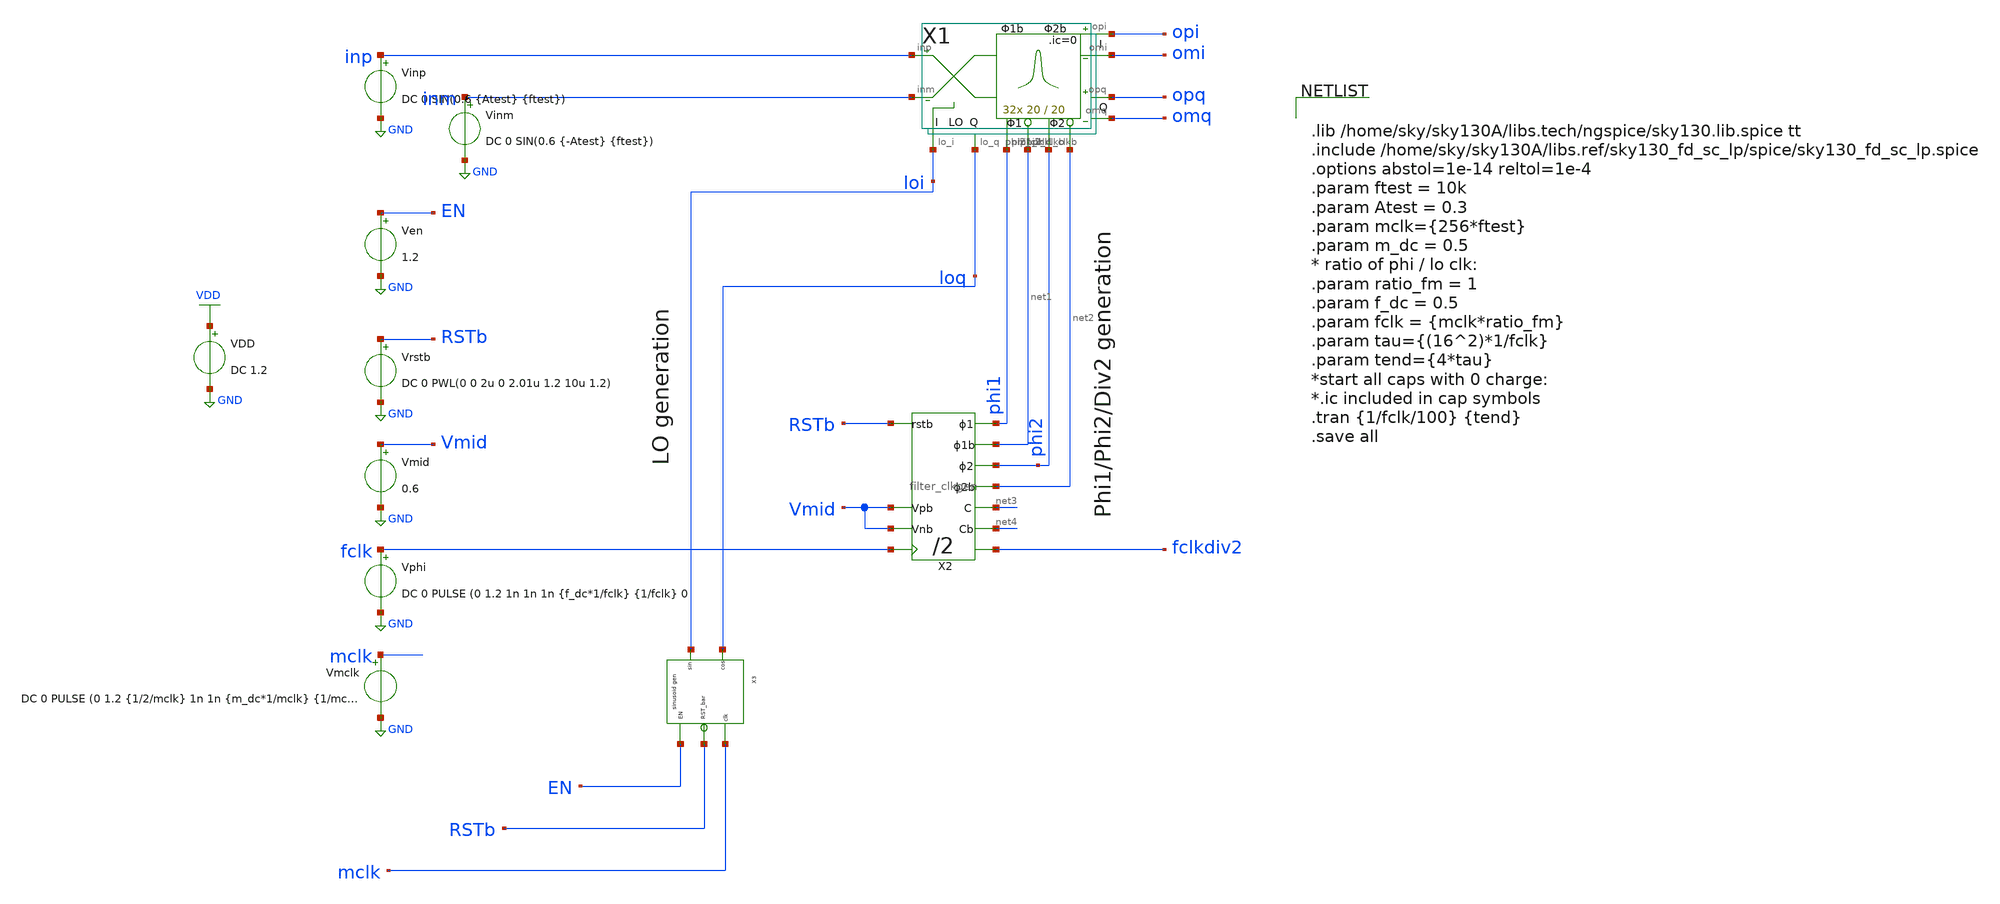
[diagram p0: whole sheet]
** sch_path: xschem/wavelet_channel/wavelet_iq_top.sch
**.subckt wavelet_iq_top
Vinp inp GND DC 0 SIN(0.6 {Atest} {ftest})
VDD VDD GND DC 1.2
Vinm inm GND DC 0 SIN(0.6 {-Atest} {ftest})
Vphi fclk GND DC 0 PULSE (0 1.2 1n 1n 1n {f_dc*1/fclk} {1/fclk} 0
X1 inp opi phi1 phi2 inm omi loi loq opq omq net2 net1 wavelet_iq W=20 L=20
X2 RSTb fclk net2 phi2 net1 phi1 net4 net3 fclkdiv2 Vmid Vmid filter_clkgen
Ven EN GND 1.2
Vrstb RSTb GND DC 0 PWL(0 0 2u 0 2.01u 1.2 10u 1.2)
Vmid Vmid GND 0.6
Vmclk mclk GND DC 0 PULSE (0 1.2 {1/2/mclk} 1n 1n {m_dc*1/mclk} {1/mclk} 0
X3 EN RSTb mclk loi loq sinusoid_generator
**** begin user architecture code


.lib /home/sky/sky130A/libs.tech/ngspice/sky130.lib.spice tt
.include /home/sky/sky130A/libs.ref/sky130_fd_sc_lp/spice/sky130_fd_sc_lp.spice
.options abstol=1e-14 reltol=1e-4
.param ftest = 10k
.param Atest = 0.3
.param mclk={256*ftest}
.param m_dc = 0.5
* ratio of phi / lo clk:
.param ratio_fm = 1
.param f_dc = 0.5
.param fclk = {mclk*ratio_fm}
.param tau={(16^2)*1/fclk}
.param tend={4*tau}
*start all caps with 0 charge:
*.ic included in cap symbols
.tran {1/fclk/100} {tend}
.save all


**** end user architecture code
**.ends
.GLOBAL GND
.GLOBAL VDD
.end
